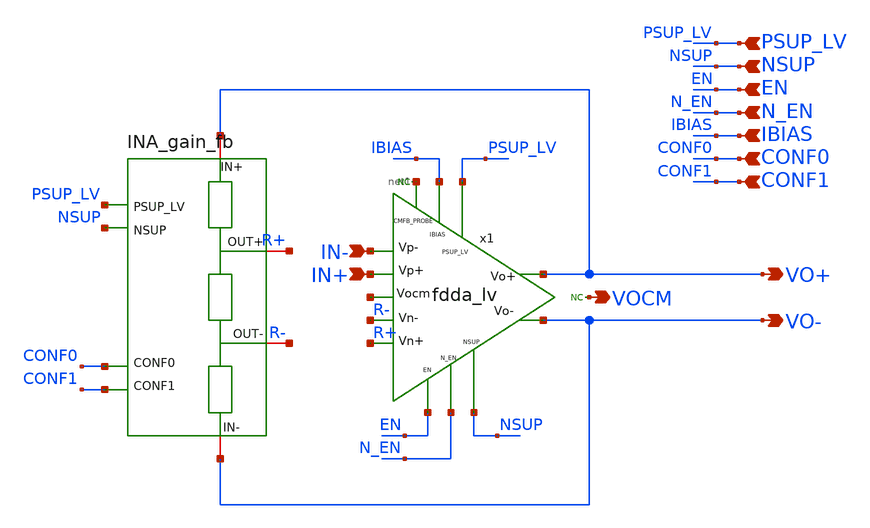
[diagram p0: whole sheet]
** sch_path: xschem/blocks/INA/INA.sch
**.subckt INA VO+ VO- IN+ IN- NSUP EN N_EN IBIAS PSUP_LV CONF0 CONF1 VOCM
*.opin VO+
*.opin VO-
*.ipin IN+
*.ipin IN-
*.ipin NSUP
*.ipin EN
*.ipin N_EN
*.ipin IBIAS
*.ipin PSUP_LV
*.ipin CONF0
*.ipin CONF1
*.opin VOCM
* noconn VOCM
* noconn #net1
x1 PSUP_LV IN- R- R+ IN+ VO+ VO- IBIAS N_EN EN NSUP net1 net2 fdda_lv
x1 VO+ R+ PSUP_LV NSUP CONF1 CONF0 R- VO- INA_gain_fb
**.ends
.end
